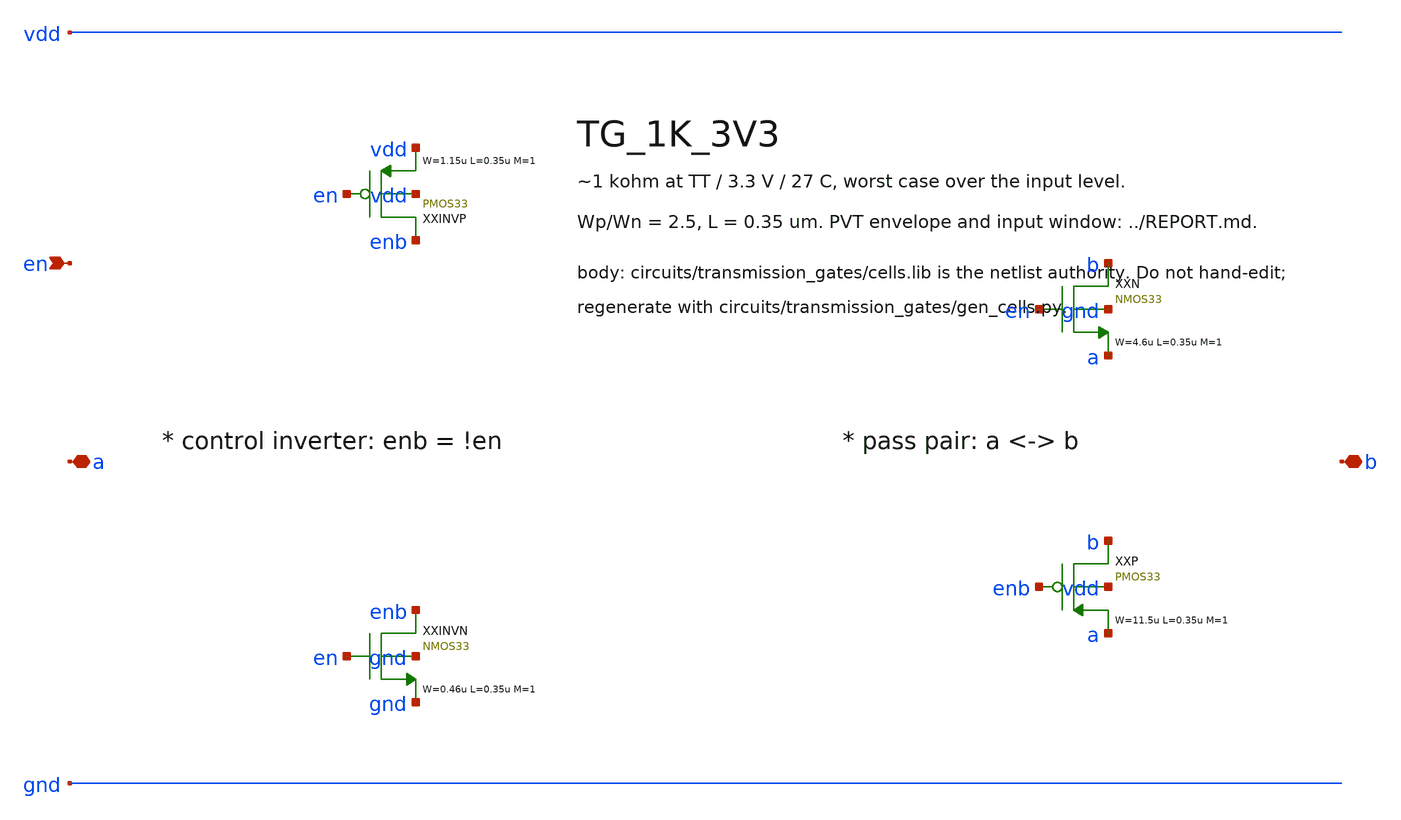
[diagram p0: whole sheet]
** sch_path: xschem/transmission_gates/TG_1K_3V3.sch
**.subckt TG_1K_3V3 a b en
*.iopin a
*.iopin b
*.ipin en
XXINVP enb en vdd vdd PMOS33 W=1.15u L=0.35u M=1 MM_SIGMA=0
XXINVN enb en gnd gnd NMOS33 W=0.46u L=0.35u M=1 MM_SIGMA=0
XXN b en a gnd NMOS33 W=4.6u L=0.35u M=1 MM_SIGMA=0
XXP b enb a vdd PMOS33 W=11.5u L=0.35u M=1 MM_SIGMA=0
**.ends
.end
